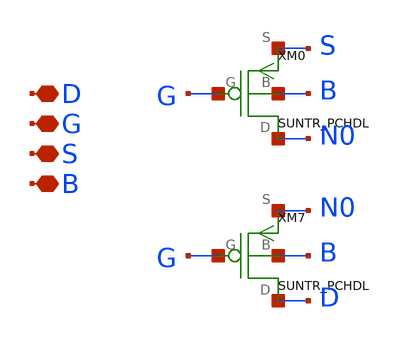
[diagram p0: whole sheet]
** sch_path: ip/sun_tr_sky130nm/design/SUN_TR_SKY130NM/SUNTR_PCHDLCM.sch
**.subckt SUNTR_PCHDLCM D G S B
*.iopin D
*.iopin G
*.iopin S
*.iopin B
XM0 N0 G S B SUNTR_PCHDL
XM7 D G N0 B SUNTR_PCHDL
**.ends
.end
